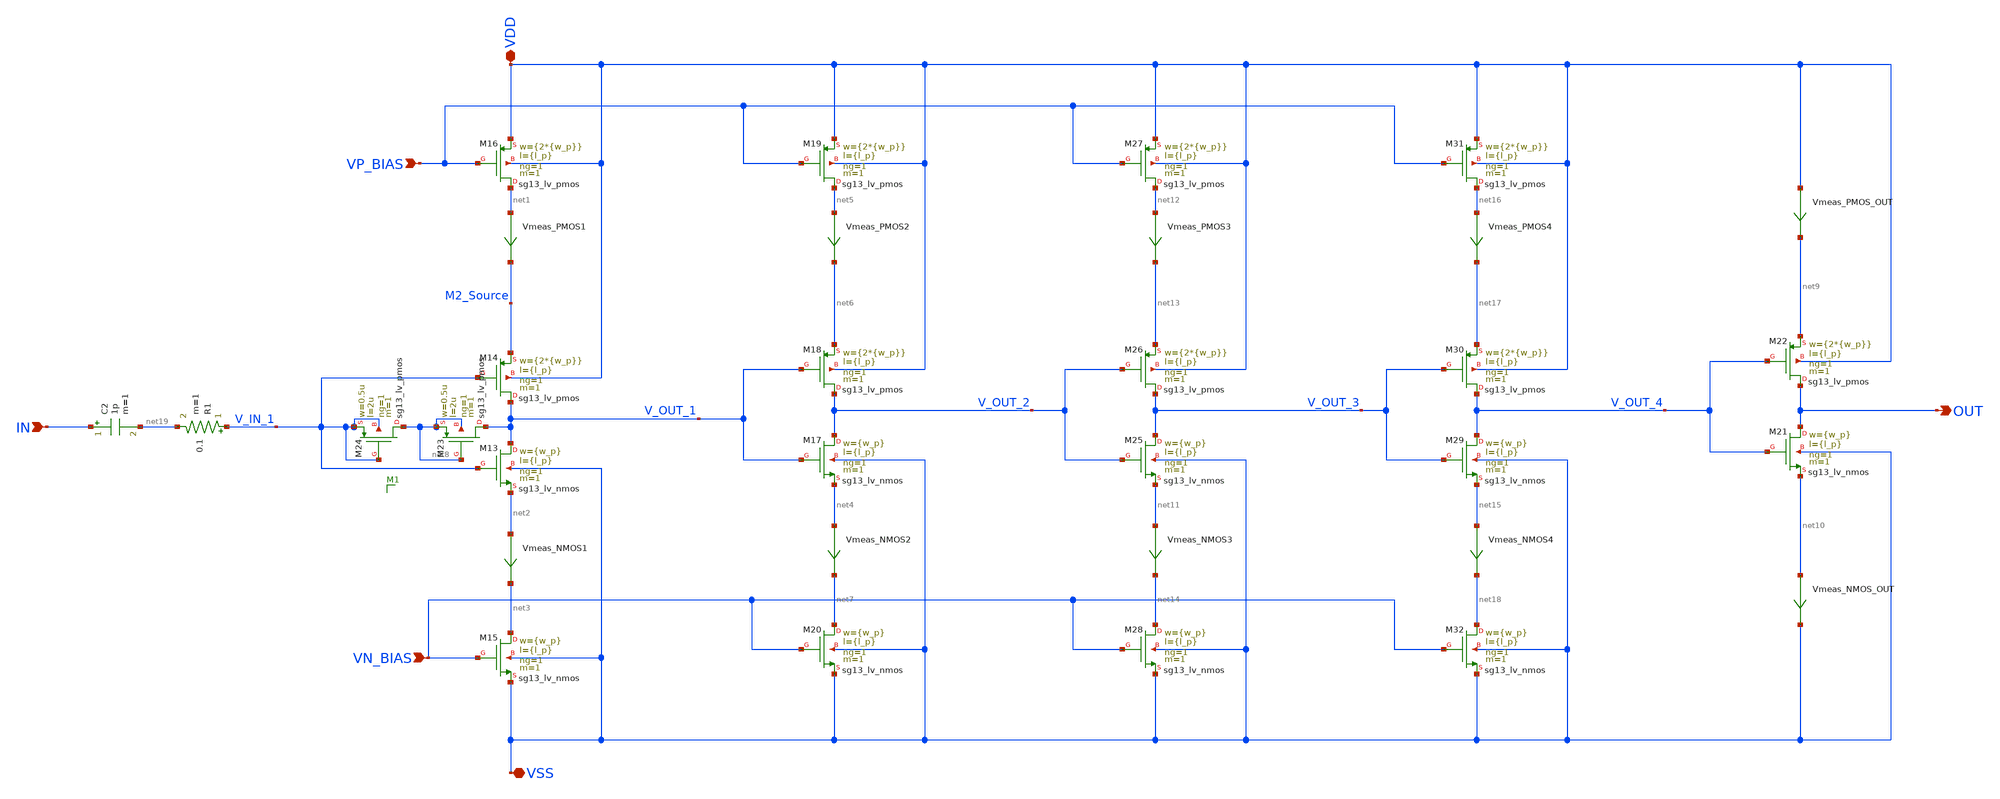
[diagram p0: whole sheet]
** sch_path: clock_gen.sch
**.subckt clock_gen IN VSS OUT VDD VP_BIAS VN_BIAS
*.ipin IN
*.iopin VSS
*.opin OUT
*.iopin VDD
*.ipin VP_BIAS
*.ipin VN_BIAS
XM13 V_OUT_1 V_IN_1 net2 VSS sg13_lv_nmos w={w_p} l={l_p} ng=1 m=1 mm_ok=1
XM14 V_OUT_1 V_IN_1 M2_Source VDD sg13_lv_pmos w={2*{w_p}} l={l_p} ng=1 m=1 mm_ok=1
XM15 net3 VN_BIAS VSS VSS sg13_lv_nmos w={w_p} l={l_p} ng=1 m=1 mm_ok=1
XM16 net1 VP_BIAS VDD VDD sg13_lv_pmos w={2*{w_p}} l={l_p} ng=1 m=1 mm_ok=1
Vmeas_PMOS1 net1 M2_Source 0
.save i(vmeas_pmos1)
Vmeas_NMOS1 net2 net3 0
.save i(vmeas_nmos1)
C2 IN net19 1p m=1
XM17 V_OUT_2 V_OUT_1 net4 VSS sg13_lv_nmos w={w_p} l={l_p} ng=1 m=1 mm_ok=1
XM18 V_OUT_2 V_OUT_1 net6 VDD sg13_lv_pmos w={2*{w_p}} l={l_p} ng=1 m=1 mm_ok=1
Vmeas_NMOS2 net4 net7 0
.save i(vmeas_nmos2)
XM19 net5 VP_BIAS VDD VDD sg13_lv_pmos w={2*{w_p}} l={l_p} ng=1 m=1 mm_ok=1
Vmeas_PMOS2 net5 net6 0
.save i(vmeas_pmos2)
XM20 net7 VN_BIAS VSS VSS sg13_lv_nmos w={w_p} l={l_p} ng=1 m=1 mm_ok=1
XM21 OUT V_OUT_4 net10 VSS sg13_lv_nmos w={w_p} l={l_p} ng=1 m=1 mm_ok=1
XM22 OUT V_OUT_4 net9 VDD sg13_lv_pmos w={2*{w_p}} l={l_p} ng=1 m=1 mm_ok=1
XM23 V_OUT_1 net8 net8 net8 sg13_lv_pmos w=0.5u l=2u ng=1 m=1 mm_ok=1
XM24 net8 V_IN_1 V_IN_1 V_IN_1 sg13_lv_pmos w=0.5u l=2u ng=1 m=1 mm_ok=1
Vmeas_PMOS_OUT VDD net9 0
.save i(vmeas_pmos_out)
Vmeas_NMOS_OUT net10 VSS 0
.save i(vmeas_nmos_out)
XM25 V_OUT_3 V_OUT_2 net11 VSS sg13_lv_nmos w={w_p} l={l_p} ng=1 m=1 mm_ok=1
XM26 V_OUT_3 V_OUT_2 net13 VDD sg13_lv_pmos w={2*{w_p}} l={l_p} ng=1 m=1 mm_ok=1
Vmeas_NMOS3 net11 net14 0
.save i(vmeas_nmos3)
XM27 net12 VP_BIAS VDD VDD sg13_lv_pmos w={2*{w_p}} l={l_p} ng=1 m=1 mm_ok=1
Vmeas_PMOS3 net12 net13 0
.save i(vmeas_pmos3)
XM28 net14 VN_BIAS VSS VSS sg13_lv_nmos w={w_p} l={l_p} ng=1 m=1 mm_ok=1
XM29 V_OUT_4 V_OUT_3 net15 VSS sg13_lv_nmos w={w_p} l={l_p} ng=1 m=1 mm_ok=1
XM30 V_OUT_4 V_OUT_3 net17 VDD sg13_lv_pmos w={2*{w_p}} l={l_p} ng=1 m=1 mm_ok=1
Vmeas_NMOS4 net15 net18 0
.save i(vmeas_nmos4)
XM31 net16 VP_BIAS VDD VDD sg13_lv_pmos w={2*{w_p}} l={l_p} ng=1 m=1 mm_ok=1
Vmeas_PMOS4 net16 net17 0
.save i(vmeas_pmos4)
XM32 net18 VN_BIAS VSS VSS sg13_lv_nmos w={w_p} l={l_p} ng=1 m=1 mm_ok=1
R1 V_IN_1 net19 0.1 m=1
**.ends
.end
